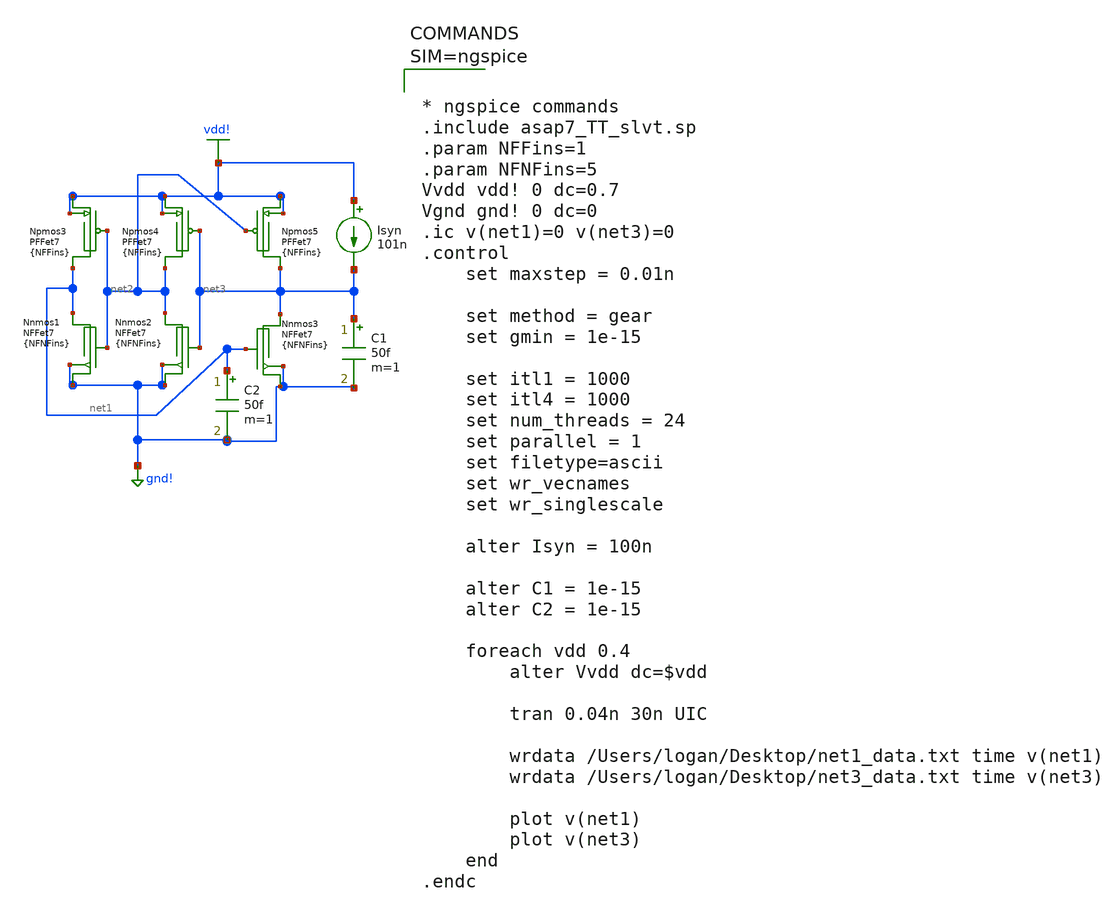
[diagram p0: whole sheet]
** sch_path: SimulationModeling/SourikopolousPlotting.sch
**.subckt SourikopolousPlotting
Npmos3 vdd! net2 net1 vdd! BSIMCMG_osdi_P nfin={NFFins}
Nnmos1 gnd! net2 net1 gnd! BSIMCMG_osdi_N nfin={NFNFins}
Npmos4 vdd! net3 net2 vdd! BSIMCMG_osdi_P nfin={NFFins}
Nnmos2 gnd! net3 net2 gnd! BSIMCMG_osdi_N nfin={NFNFins}
Npmos5 vdd! net2 net3 vdd! BSIMCMG_osdi_P nfin={NFFins}
Nnmos3 gnd! net1 net3 gnd! BSIMCMG_osdi_N nfin={NFNFins}
Isyn vdd! net3 101n
C2 net1 gnd! 50f m=1
C1 net3 gnd! 50f m=1
**** begin user architecture code



* ngspice commands
.include asap7_TT_slvt.sp
.param NFFins=1
.param NFNFins=5
Vvdd vdd! 0 dc=0.7
Vgnd gnd! 0 dc=0
.ic v(net1)=0 v(net3)=0
.control
    set maxstep = 0.01n

    set method = gear
    set gmin = 1e-15

    set itl1 = 1000
    set itl4 = 1000
    set num_threads = 24
    set parallel = 1
    set filetype=ascii
    set wr_vecnames
    set wr_singlescale

    alter Isyn = 100n

    alter C1 = 1e-15
    alter C2 = 1e-15

    foreach vdd 0.4
        alter Vvdd dc=$vdd

        tran 0.04n 30n UIC

        wrdata /Users/logan/Desktop/net1_data.txt time v(net1)
        wrdata /Users/logan/Desktop/net3_data.txt time v(net3)

        plot v(net1)
        plot v(net3)
    end
.endc



**** end user architecture code
**.ends
.GLOBAL vdd!
.GLOBAL gnd!
.end
